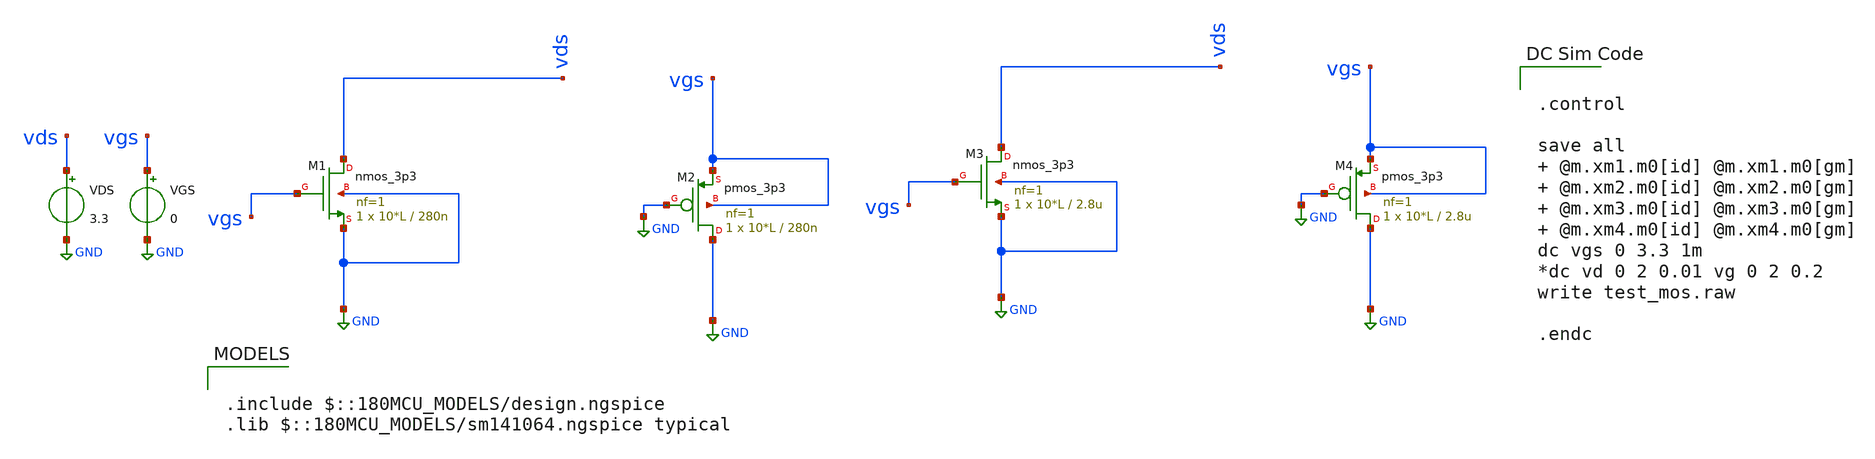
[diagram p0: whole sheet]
** sch_path: ITI_Labs/Lab1/MOS/Design/MOS_Testbench.sch
**.subckt MOS_Testbench
XM1 vds vgs GND GND nmos_3p3 L=280n W=10*L nf=1 ad='int((nf+1)/2) * W/nf * 0.18u' as='int((nf+2)/2) * W/nf * 0.18u'
+ pd='2*int((nf+1)/2) * (W/nf + 0.18u)' ps='2*int((nf+2)/2) * (W/nf + 0.18u)' nrd='0.18u / W' nrs='0.18u / W'
+ sa=0 sb=0 sd=0 m=1
XM2 GND GND vgs vgs pmos_3p3 L=280n W=10*L nf=1 ad='int((nf+1)/2) * W/nf * 0.18u' as='int((nf+2)/2) * W/nf * 0.18u'
+ pd='2*int((nf+1)/2) * (W/nf + 0.18u)' ps='2*int((nf+2)/2) * (W/nf + 0.18u)' nrd='0.18u / W' nrs='0.18u / W'
+ sa=0 sb=0 sd=0 m=1
VDS vds GND 3.3
VGS vgs GND 0
XM3 vds vgs GND GND nmos_3p3 L=2.8u W=10*L nf=1 ad='int((nf+1)/2) * W/nf * 0.18u' as='int((nf+2)/2) * W/nf * 0.18u'
+ pd='2*int((nf+1)/2) * (W/nf + 0.18u)' ps='2*int((nf+2)/2) * (W/nf + 0.18u)' nrd='0.18u / W' nrs='0.18u / W'
+ sa=0 sb=0 sd=0 m=1
XM4 GND GND vgs vgs pmos_3p3 L=2.8u W=10*L nf=1 ad='int((nf+1)/2) * W/nf * 0.18u' as='int((nf+2)/2) * W/nf * 0.18u'
+ pd='2*int((nf+1)/2) * (W/nf + 0.18u)' ps='2*int((nf+2)/2) * (W/nf + 0.18u)' nrd='0.18u / W' nrs='0.18u / W'
+ sa=0 sb=0 sd=0 m=1
**** begin user architecture code

.include $::180MCU_MODELS/design.ngspice
.lib $::180MCU_MODELS/sm141064.ngspice typical



.control

save all   @m.xm1.m0[id] @m.xm1.m0[gm]  @m.xm2.m0[id] @m.xm2.m0[gm]  @m.xm3.m0[id] @m.xm3.m0[gm]
+  @m.xm4.m0[id] @m.xm4.m0[gm]
dc vgs 0 3.3 1m
*dc vd 0 2 0.01 vg 0 2 0.2
write test_mos.raw

.endc


**** end user architecture code
**.ends
.GLOBAL GND
.end
